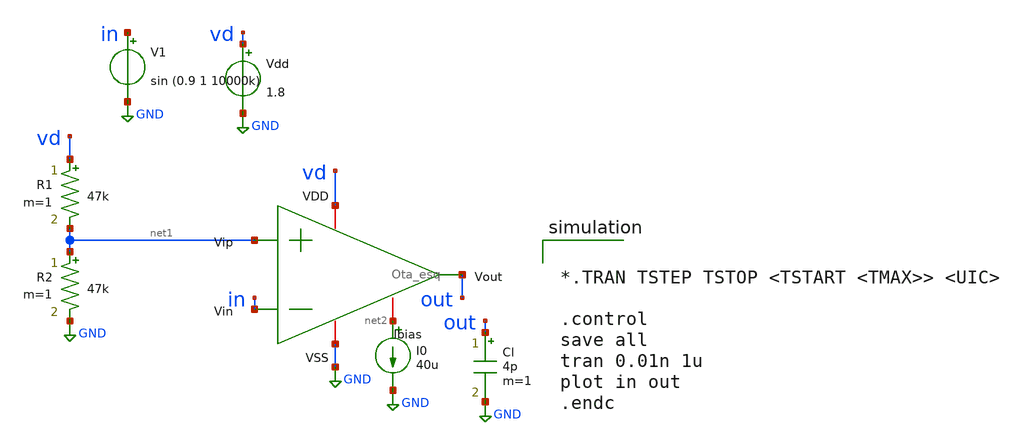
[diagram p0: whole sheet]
** sch_path: xschem/ota-tb-tran.sch
**.subckt ota-tb-tran
x1 vd in net1 out net2 GND Ota_esq
R1 vd net1 47k m=1
R2 net1 GND 47k m=1
Vdd vd GND 1.8
I0 net2 GND 40u
V1 in GND sin (0.9 1 10000k)
Cl out GND 4p m=1
**** begin user architecture code

** opencircuitdesign pdks install
.lib $::SKYWATER_MODELS/sky130.lib.spice tt_mm




*.TRAN TSTEP TSTOP <TSTART <TMAX>> <UIC>

.control
save all
tran 0.01n 1u
plot in out
.endc


**** end user architecture code
**.ends

* expanding   symbol:  /foss/designs/ota-edson/Ota_esq.sym # of pins=6
** sym_path: /foss/designs/ota-edson/Ota_esq.sym
** sch_path: /foss/designs/ota-edson/Ota_esq.sch
.subckt Ota_esq VDD Vin Vip Vout Ibias VSS
*.ipin Vin
*.ipin Vip
*.iopin VDD
*.iopin VSS
*.iopin Ibias
*.opin Vout
XM1 net1 Vin net3 net3 sky130_fd_pr__pfet_01v8 L=0.25 W=2.899 nf=1 ad='int((nf+1)/2) * W/nf * 0.29' as='int((nf+2)/2) * W/nf * 0.29'
+ pd='2*int((nf+1)/2) * (W/nf + 0.29)' ps='2*int((nf+2)/2) * (W/nf + 0.29)' nrd='0.29 / W' nrs='0.29 / W'
+ sa=0 sb=0 sd=0 mult=1 m=1
XM2 net2 Vip net3 net3 sky130_fd_pr__pfet_01v8 L=0.25 W=2.899 nf=1 ad='int((nf+1)/2) * W/nf * 0.29' as='int((nf+2)/2) * W/nf * 0.29'
+ pd='2*int((nf+1)/2) * (W/nf + 0.29)' ps='2*int((nf+2)/2) * (W/nf + 0.29)' nrd='0.29 / W' nrs='0.29 / W'
+ sa=0 sb=0 sd=0 mult=1 m=1
XM3 net1 net1 VSS VSS sky130_fd_pr__nfet_01v8 L=0.25 W=0.667 nf=1 ad='int((nf+1)/2) * W/nf * 0.29' as='int((nf+2)/2) * W/nf * 0.29'
+ pd='2*int((nf+1)/2) * (W/nf + 0.29)' ps='2*int((nf+2)/2) * (W/nf + 0.29)' nrd='0.29 / W' nrs='0.29 / W'
+ sa=0 sb=0 sd=0 mult=1 m=1
XM4 net2 net1 VSS VSS sky130_fd_pr__nfet_01v8 L=0.25 W=0.667 nf=1 ad='int((nf+1)/2) * W/nf * 0.29' as='int((nf+2)/2) * W/nf * 0.29'
+ pd='2*int((nf+1)/2) * (W/nf + 0.29)' ps='2*int((nf+2)/2) * (W/nf + 0.29)' nrd='0.29 / W' nrs='0.29 / W'
+ sa=0 sb=0 sd=0 mult=1 m=1
XM5 net3 Ibias VDD VDD sky130_fd_pr__pfet_01v8 L=0.25 W=3.333 nf=1 ad='int((nf+1)/2) * W/nf * 0.29' as='int((nf+2)/2) * W/nf * 0.29'
+ pd='2*int((nf+1)/2) * (W/nf + 0.29)' ps='2*int((nf+2)/2) * (W/nf + 0.29)' nrd='0.29 / W' nrs='0.29 / W'
+ sa=0 sb=0 sd=0 mult=1 m=1
XM8 Ibias Ibias VDD VDD sky130_fd_pr__pfet_01v8 L=0.25 W=3.333 nf=1 ad='int((nf+1)/2) * W/nf * 0.29'
+ as='int((nf+2)/2) * W/nf * 0.29' pd='2*int((nf+1)/2) * (W/nf + 0.29)' ps='2*int((nf+2)/2) * (W/nf + 0.29)'
+ nrd='0.29 / W' nrs='0.29 / W' sa=0 sb=0 sd=0 mult=1 m=1
XM6 Vout Ibias VDD VDD sky130_fd_pr__pfet_01v8 L=0.25 W=17.279 nf=1 ad='int((nf+1)/2) * W/nf * 0.29'
+ as='int((nf+2)/2) * W/nf * 0.29' pd='2*int((nf+1)/2) * (W/nf + 0.29)' ps='2*int((nf+2)/2) * (W/nf + 0.29)'
+ nrd='0.29 / W' nrs='0.29 / W' sa=0 sb=0 sd=0 mult=1 m=1
XM7 Vout net2 VSS VSS sky130_fd_pr__nfet_01v8 L=0.25 W=6.192 nf=1 ad='int((nf+1)/2) * W/nf * 0.29' as='int((nf+2)/2) * W/nf * 0.29'
+ pd='2*int((nf+1)/2) * (W/nf + 0.29)' ps='2*int((nf+2)/2) * (W/nf + 0.29)' nrd='0.29 / W' nrs='0.29 / W'
+ sa=0 sb=0 sd=0 mult=1 m=1
XC1 net2 Vout sky130_fd_pr__cap_mim_m3_1 W=23 L=23 MF=1 m=1
.ends

.GLOBAL GND
.end
